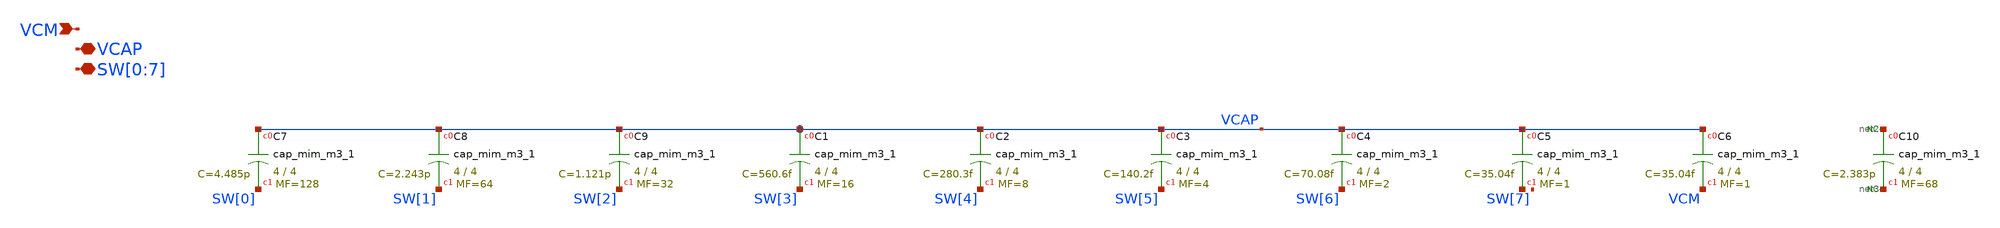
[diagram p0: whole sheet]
** sch_path: xschem/8b_cap_array.sch
**.subckt 8b_cap_array SW[0],SW[1],SW[2],SW[3],SW[4],SW[5],SW[6],SW[7] VCAP VCM
*.iopin SW[0],SW[1],SW[2],SW[3],SW[4],SW[5],SW[6],SW[7]
*.iopin VCAP
*.ipin VCM
XC1 VCAP SW[3] sky130_fd_pr__cap_mim_m3_1 W=4 L=4 MF=16 m=16
XC2 VCAP SW[4] sky130_fd_pr__cap_mim_m3_1 W=4 L=4 MF=8 m=8
XC3 VCAP SW[5] sky130_fd_pr__cap_mim_m3_1 W=4 L=4 MF=4 m=4
XC4 VCAP SW[6] sky130_fd_pr__cap_mim_m3_1 W=4 L=4 MF=2 m=2
XC5 VCAP net1 sky130_fd_pr__cap_mim_m3_1 W=4 L=4 MF=1 m=1
XC6 VCAP VCM sky130_fd_pr__cap_mim_m3_1 W=4 L=4 MF=1 m=1
XC7 VCAP SW[0] sky130_fd_pr__cap_mim_m3_1 W=4 L=4 MF=128 m=128
XC8 VCAP SW[1] sky130_fd_pr__cap_mim_m3_1 W=4 L=4 MF=64 m=64
XC9 VCAP SW[2] sky130_fd_pr__cap_mim_m3_1 W=4 L=4 MF=32 m=32
XC10 net2 net3 sky130_fd_pr__cap_mim_m3_1 W=4 L=4 MF=68 m=68
* noconn #net2
* noconn #net3
**.ends
.end
